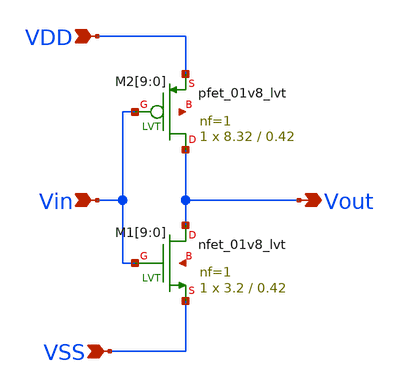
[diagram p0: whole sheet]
** sch_path: design/THESIS_EXP_RO_INVERTER_SKY130A/INV_LVT_v2.sch
**.subckt INV_LVT_v2 VDD VSS Vin Vout
*.ipin VDD
*.ipin VSS
*.ipin Vin
*.opin Vout
XM1[9] Vout Vin VSS net1[9] sky130_fd_pr__nfet_01v8_lvt L=0.42 W=3.2 nf=1 ad='int((nf+1)/2) * W/nf * 0.29'
+ as='int((nf+2)/2) * W/nf * 0.29' pd='2*int((nf+1)/2) * (W/nf + 0.29)' ps='2*int((nf+2)/2) * (W/nf + 0.29)'
+ nrd='0.29 / W' nrs='0.29 / W' sa=0 sb=0 sd=0 mult=1 m=1
XM1[8] Vout Vin VSS net1[8] sky130_fd_pr__nfet_01v8_lvt L=0.42 W=3.2 nf=1 ad='int((nf+1)/2) * W/nf * 0.29'
+ as='int((nf+2)/2) * W/nf * 0.29' pd='2*int((nf+1)/2) * (W/nf + 0.29)' ps='2*int((nf+2)/2) * (W/nf + 0.29)'
+ nrd='0.29 / W' nrs='0.29 / W' sa=0 sb=0 sd=0 mult=1 m=1
XM1[7] Vout Vin VSS net1[7] sky130_fd_pr__nfet_01v8_lvt L=0.42 W=3.2 nf=1 ad='int((nf+1)/2) * W/nf * 0.29'
+ as='int((nf+2)/2) * W/nf * 0.29' pd='2*int((nf+1)/2) * (W/nf + 0.29)' ps='2*int((nf+2)/2) * (W/nf + 0.29)'
+ nrd='0.29 / W' nrs='0.29 / W' sa=0 sb=0 sd=0 mult=1 m=1
XM1[6] Vout Vin VSS net1[6] sky130_fd_pr__nfet_01v8_lvt L=0.42 W=3.2 nf=1 ad='int((nf+1)/2) * W/nf * 0.29'
+ as='int((nf+2)/2) * W/nf * 0.29' pd='2*int((nf+1)/2) * (W/nf + 0.29)' ps='2*int((nf+2)/2) * (W/nf + 0.29)'
+ nrd='0.29 / W' nrs='0.29 / W' sa=0 sb=0 sd=0 mult=1 m=1
XM1[5] Vout Vin VSS net1[5] sky130_fd_pr__nfet_01v8_lvt L=0.42 W=3.2 nf=1 ad='int((nf+1)/2) * W/nf * 0.29'
+ as='int((nf+2)/2) * W/nf * 0.29' pd='2*int((nf+1)/2) * (W/nf + 0.29)' ps='2*int((nf+2)/2) * (W/nf + 0.29)'
+ nrd='0.29 / W' nrs='0.29 / W' sa=0 sb=0 sd=0 mult=1 m=1
XM1[4] Vout Vin VSS net1[4] sky130_fd_pr__nfet_01v8_lvt L=0.42 W=3.2 nf=1 ad='int((nf+1)/2) * W/nf * 0.29'
+ as='int((nf+2)/2) * W/nf * 0.29' pd='2*int((nf+1)/2) * (W/nf + 0.29)' ps='2*int((nf+2)/2) * (W/nf + 0.29)'
+ nrd='0.29 / W' nrs='0.29 / W' sa=0 sb=0 sd=0 mult=1 m=1
XM1[3] Vout Vin VSS net1[3] sky130_fd_pr__nfet_01v8_lvt L=0.42 W=3.2 nf=1 ad='int((nf+1)/2) * W/nf * 0.29'
+ as='int((nf+2)/2) * W/nf * 0.29' pd='2*int((nf+1)/2) * (W/nf + 0.29)' ps='2*int((nf+2)/2) * (W/nf + 0.29)'
+ nrd='0.29 / W' nrs='0.29 / W' sa=0 sb=0 sd=0 mult=1 m=1
XM1[2] Vout Vin VSS net1[2] sky130_fd_pr__nfet_01v8_lvt L=0.42 W=3.2 nf=1 ad='int((nf+1)/2) * W/nf * 0.29'
+ as='int((nf+2)/2) * W/nf * 0.29' pd='2*int((nf+1)/2) * (W/nf + 0.29)' ps='2*int((nf+2)/2) * (W/nf + 0.29)'
+ nrd='0.29 / W' nrs='0.29 / W' sa=0 sb=0 sd=0 mult=1 m=1
XM1[1] Vout Vin VSS net1[1] sky130_fd_pr__nfet_01v8_lvt L=0.42 W=3.2 nf=1 ad='int((nf+1)/2) * W/nf * 0.29'
+ as='int((nf+2)/2) * W/nf * 0.29' pd='2*int((nf+1)/2) * (W/nf + 0.29)' ps='2*int((nf+2)/2) * (W/nf + 0.29)'
+ nrd='0.29 / W' nrs='0.29 / W' sa=0 sb=0 sd=0 mult=1 m=1
XM1[0] Vout Vin VSS net1[0] sky130_fd_pr__nfet_01v8_lvt L=0.42 W=3.2 nf=1 ad='int((nf+1)/2) * W/nf * 0.29'
+ as='int((nf+2)/2) * W/nf * 0.29' pd='2*int((nf+1)/2) * (W/nf + 0.29)' ps='2*int((nf+2)/2) * (W/nf + 0.29)'
+ nrd='0.29 / W' nrs='0.29 / W' sa=0 sb=0 sd=0 mult=1 m=1
XM2[9] Vout Vin VDD net2[9] sky130_fd_pr__pfet_01v8_lvt L=0.42 W=8.32 nf=1 ad='int((nf+1)/2) * W/nf * 0.29'
+ as='int((nf+2)/2) * W/nf * 0.29' pd='2*int((nf+1)/2) * (W/nf + 0.29)' ps='2*int((nf+2)/2) * (W/nf + 0.29)'
+ nrd='0.29 / W' nrs='0.29 / W' sa=0 sb=0 sd=0 mult=1 m=1
XM2[8] Vout Vin VDD net2[8] sky130_fd_pr__pfet_01v8_lvt L=0.42 W=8.32 nf=1 ad='int((nf+1)/2) * W/nf * 0.29'
+ as='int((nf+2)/2) * W/nf * 0.29' pd='2*int((nf+1)/2) * (W/nf + 0.29)' ps='2*int((nf+2)/2) * (W/nf + 0.29)'
+ nrd='0.29 / W' nrs='0.29 / W' sa=0 sb=0 sd=0 mult=1 m=1
XM2[7] Vout Vin VDD net2[7] sky130_fd_pr__pfet_01v8_lvt L=0.42 W=8.32 nf=1 ad='int((nf+1)/2) * W/nf * 0.29'
+ as='int((nf+2)/2) * W/nf * 0.29' pd='2*int((nf+1)/2) * (W/nf + 0.29)' ps='2*int((nf+2)/2) * (W/nf + 0.29)'
+ nrd='0.29 / W' nrs='0.29 / W' sa=0 sb=0 sd=0 mult=1 m=1
XM2[6] Vout Vin VDD net2[6] sky130_fd_pr__pfet_01v8_lvt L=0.42 W=8.32 nf=1 ad='int((nf+1)/2) * W/nf * 0.29'
+ as='int((nf+2)/2) * W/nf * 0.29' pd='2*int((nf+1)/2) * (W/nf + 0.29)' ps='2*int((nf+2)/2) * (W/nf + 0.29)'
+ nrd='0.29 / W' nrs='0.29 / W' sa=0 sb=0 sd=0 mult=1 m=1
XM2[5] Vout Vin VDD net2[5] sky130_fd_pr__pfet_01v8_lvt L=0.42 W=8.32 nf=1 ad='int((nf+1)/2) * W/nf * 0.29'
+ as='int((nf+2)/2) * W/nf * 0.29' pd='2*int((nf+1)/2) * (W/nf + 0.29)' ps='2*int((nf+2)/2) * (W/nf + 0.29)'
+ nrd='0.29 / W' nrs='0.29 / W' sa=0 sb=0 sd=0 mult=1 m=1
XM2[4] Vout Vin VDD net2[4] sky130_fd_pr__pfet_01v8_lvt L=0.42 W=8.32 nf=1 ad='int((nf+1)/2) * W/nf * 0.29'
+ as='int((nf+2)/2) * W/nf * 0.29' pd='2*int((nf+1)/2) * (W/nf + 0.29)' ps='2*int((nf+2)/2) * (W/nf + 0.29)'
+ nrd='0.29 / W' nrs='0.29 / W' sa=0 sb=0 sd=0 mult=1 m=1
XM2[3] Vout Vin VDD net2[3] sky130_fd_pr__pfet_01v8_lvt L=0.42 W=8.32 nf=1 ad='int((nf+1)/2) * W/nf * 0.29'
+ as='int((nf+2)/2) * W/nf * 0.29' pd='2*int((nf+1)/2) * (W/nf + 0.29)' ps='2*int((nf+2)/2) * (W/nf + 0.29)'
+ nrd='0.29 / W' nrs='0.29 / W' sa=0 sb=0 sd=0 mult=1 m=1
XM2[2] Vout Vin VDD net2[2] sky130_fd_pr__pfet_01v8_lvt L=0.42 W=8.32 nf=1 ad='int((nf+1)/2) * W/nf * 0.29'
+ as='int((nf+2)/2) * W/nf * 0.29' pd='2*int((nf+1)/2) * (W/nf + 0.29)' ps='2*int((nf+2)/2) * (W/nf + 0.29)'
+ nrd='0.29 / W' nrs='0.29 / W' sa=0 sb=0 sd=0 mult=1 m=1
XM2[1] Vout Vin VDD net2[1] sky130_fd_pr__pfet_01v8_lvt L=0.42 W=8.32 nf=1 ad='int((nf+1)/2) * W/nf * 0.29'
+ as='int((nf+2)/2) * W/nf * 0.29' pd='2*int((nf+1)/2) * (W/nf + 0.29)' ps='2*int((nf+2)/2) * (W/nf + 0.29)'
+ nrd='0.29 / W' nrs='0.29 / W' sa=0 sb=0 sd=0 mult=1 m=1
XM2[0] Vout Vin VDD net2[0] sky130_fd_pr__pfet_01v8_lvt L=0.42 W=8.32 nf=1 ad='int((nf+1)/2) * W/nf * 0.29'
+ as='int((nf+2)/2) * W/nf * 0.29' pd='2*int((nf+1)/2) * (W/nf + 0.29)' ps='2*int((nf+2)/2) * (W/nf + 0.29)'
+ nrd='0.29 / W' nrs='0.29 / W' sa=0 sb=0 sd=0 mult=1 m=1
**.ends
.end
